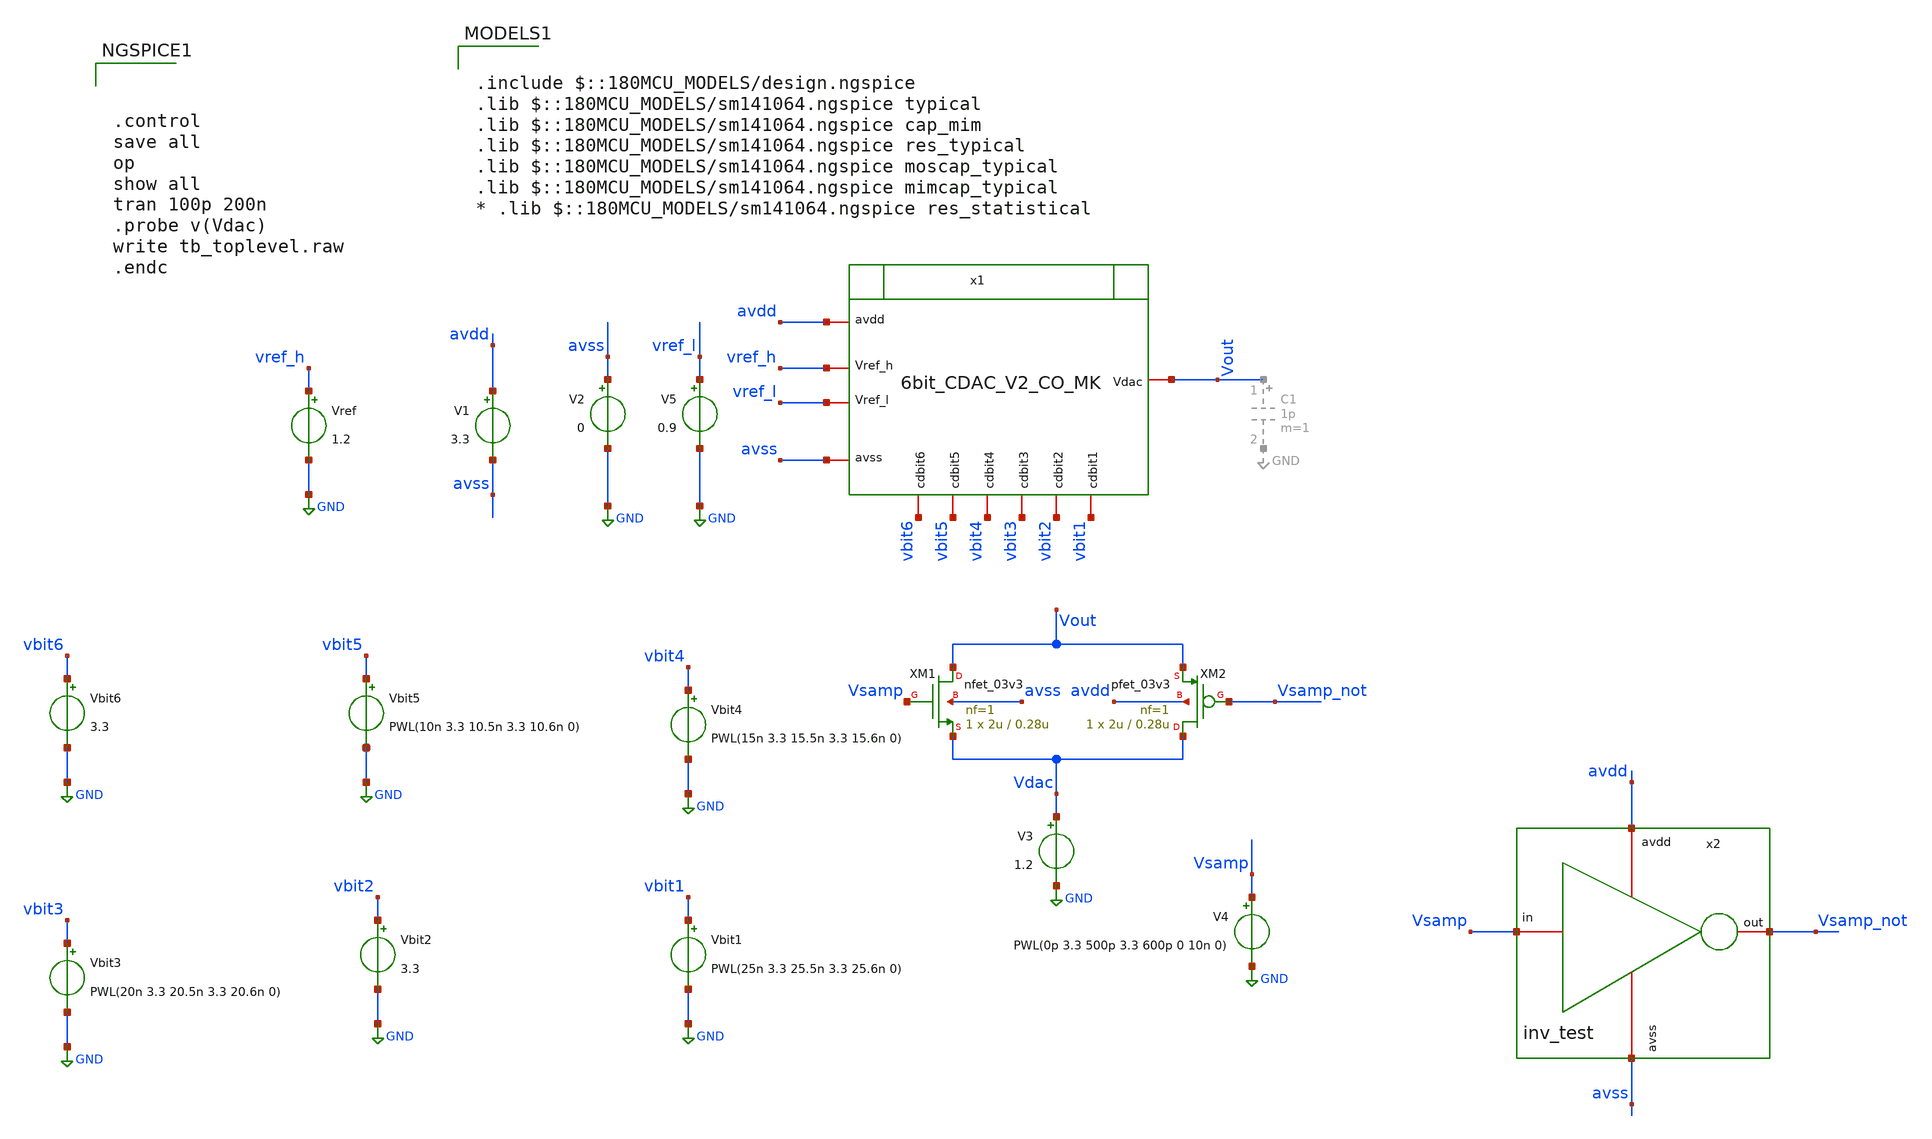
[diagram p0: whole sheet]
** sch_path: designs/full_ADC/tb_toplevel.sch
**.subckt tb_toplevel
V1 avdd avss 3.3
V2 avss GND 0
Vbit1 vbit1 GND PWL(25n 3.3 25.5n 3.3 25.6n 0)
Vbit2 vbit2 GND 3.3
Vbit3 vbit3 GND PWL(20n 3.3 20.5n 3.3 20.6n 0)
Vbit4 vbit4 GND PWL(15n 3.3 15.5n 3.3 15.6n 0)
Vbit5 vbit5 GND PWL(10n 3.3 10.5n 3.3 10.6n 0)
Vbit6 vbit6 GND 3.3
Vref vref_h GND 1.2
V3 Vdac GND 1.2
XM1 Vout Vsamp Vdac avss nfet_03v3 L=0.28u W=2u nf=1 ad='int((nf+1)/2) * W/nf * 0.18u' as='int((nf+2)/2) * W/nf * 0.18u'
+ pd='2*int((nf+1)/2) * (W/nf + 0.18u)' ps='2*int((nf+2)/2) * (W/nf + 0.18u)' nrd='0.18u / W' nrs='0.18u / W'
+ sa=0 sb=0 sd=0 m=1
XM2 Vdac Vsamp_not Vout avdd pfet_03v3 L=0.28u W=2u nf=1 ad='int((nf+1)/2) * W/nf * 0.18u' as='int((nf+2)/2) * W/nf * 0.18u'
+ pd='2*int((nf+1)/2) * (W/nf + 0.18u)' ps='2*int((nf+2)/2) * (W/nf + 0.18u)' nrd='0.18u / W' nrs='0.18u / W'
+ sa=0 sb=0 sd=0 m=1
x2 avdd Vsamp Vsamp_not avss inv_test
V4 Vsamp GND PWL(0p 3.3 500p 3.3 600p 0 10n 0)
V5 vref_l GND 0.9
**** begin user architecture code



.control
save all
op
show all
tran 100p 200n
.probe v(Vdac)
write tb_toplevel.raw
.endc



.include $::180MCU_MODELS/design.ngspice
.lib $::180MCU_MODELS/sm141064.ngspice typical
.lib $::180MCU_MODELS/sm141064.ngspice cap_mim
.lib $::180MCU_MODELS/sm141064.ngspice res_typical
.lib $::180MCU_MODELS/sm141064.ngspice moscap_typical
.lib $::180MCU_MODELS/sm141064.ngspice mimcap_typical
* .lib $::180MCU_MODELS/sm141064.ngspice res_statistical

**** end user architecture code
**.ends

* expanding   symbol:  libs/WK_Kadam/inv_test.sym # of pins=4
** sym_path: libs/WK_Kadam/inv_test.sym
** sch_path: libs/WK_Kadam/inv_test.sch
.subckt inv_test avdd in out avss
*.iopin avdd
*.iopin avss
*.iopin in
*.iopin out
XM3 out in avss avss nfet_03v3 L=0.28u W=1u nf=1 ad='int((nf+1)/2) * W/nf * 0.18u' as='int((nf+2)/2) * W/nf * 0.18u'
+ pd='2*int((nf+1)/2) * (W/nf + 0.18u)' ps='2*int((nf+2)/2) * (W/nf + 0.18u)' nrd='0.18u / W' nrs='0.18u / W'
+ sa=0 sb=0 sd=0 m=1
XM4 out in avdd avdd pfet_03v3 L=0.28u W=2.5u nf=1 ad='int((nf+1)/2) * W/nf * 0.18u' as='int((nf+2)/2) * W/nf * 0.18u'
+ pd='2*int((nf+1)/2) * (W/nf + 0.18u)' ps='2*int((nf+2)/2) * (W/nf + 0.18u)' nrd='0.18u / W' nrs='0.18u / W'
+ sa=0 sb=0 sd=0 m=1
.ends

.GLOBAL GND
.end
